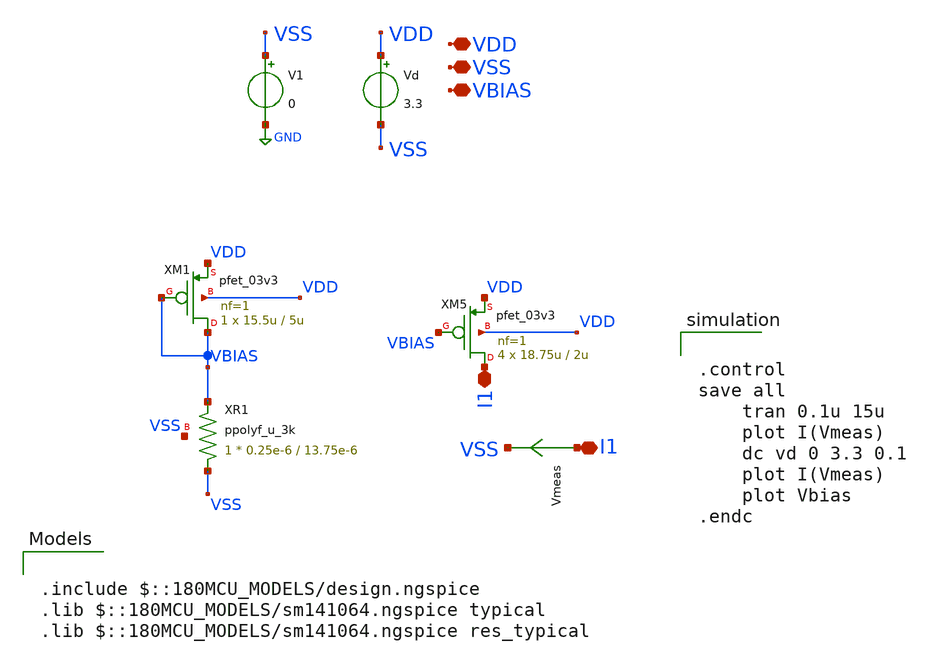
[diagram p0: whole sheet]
** sch_path: designs/startup_pb.sch
**.subckt startup_pb VDD VSS VBIAS I1 I1
*.iopin VDD
*.iopin VSS
*.iopin VBIAS
*.iopin I1
*.iopin I1
XR1 VSS VBIAS VSS ppolyf_u_3k r_width=0.25e-6 r_length=13.75e-6 m=1
XM1 VBIAS VBIAS VDD VDD pfet_03v3 L=5u W=15.5u nf=1 ad='int((nf+1)/2) * W/nf * 0.18u' as='int((nf+2)/2) * W/nf * 0.18u'
+ pd='2*int((nf+1)/2) * (W/nf + 0.18u)' ps='2*int((nf+2)/2) * (W/nf + 0.18u)' nrd='0.18u / W' nrs='0.18u / W'
+ sa=0 sb=0 sd=0 m=1
XM5 I1 VBIAS VDD VDD pfet_03v3 L=2u W=18.75u nf=1 ad='int((nf+1)/2) * W/nf * 0.18u' as='int((nf+2)/2) * W/nf * 0.18u'
+ pd='2*int((nf+1)/2) * (W/nf + 0.18u)' ps='2*int((nf+2)/2) * (W/nf + 0.18u)' nrd='0.18u / W' nrs='0.18u / W'
+ sa=0 sb=0 sd=0 m=4
Vmeas I1 VSS 0
.save i(vmeas)
Vd VDD VSS 3.3
V1 VSS GND 0
**** begin user architecture code

.include $::180MCU_MODELS/design.ngspice
.lib $::180MCU_MODELS/sm141064.ngspice typical
.lib $::180MCU_MODELS/sm141064.ngspice res_typical



.control
save all
	tran 0.1u 15u
	plot I(Vmeas)
	dc vd 0 3.3 0.1
	plot I(Vmeas)
	plot Vbias
.endc


**** end user architecture code
**.ends
.GLOBAL GND
.end
